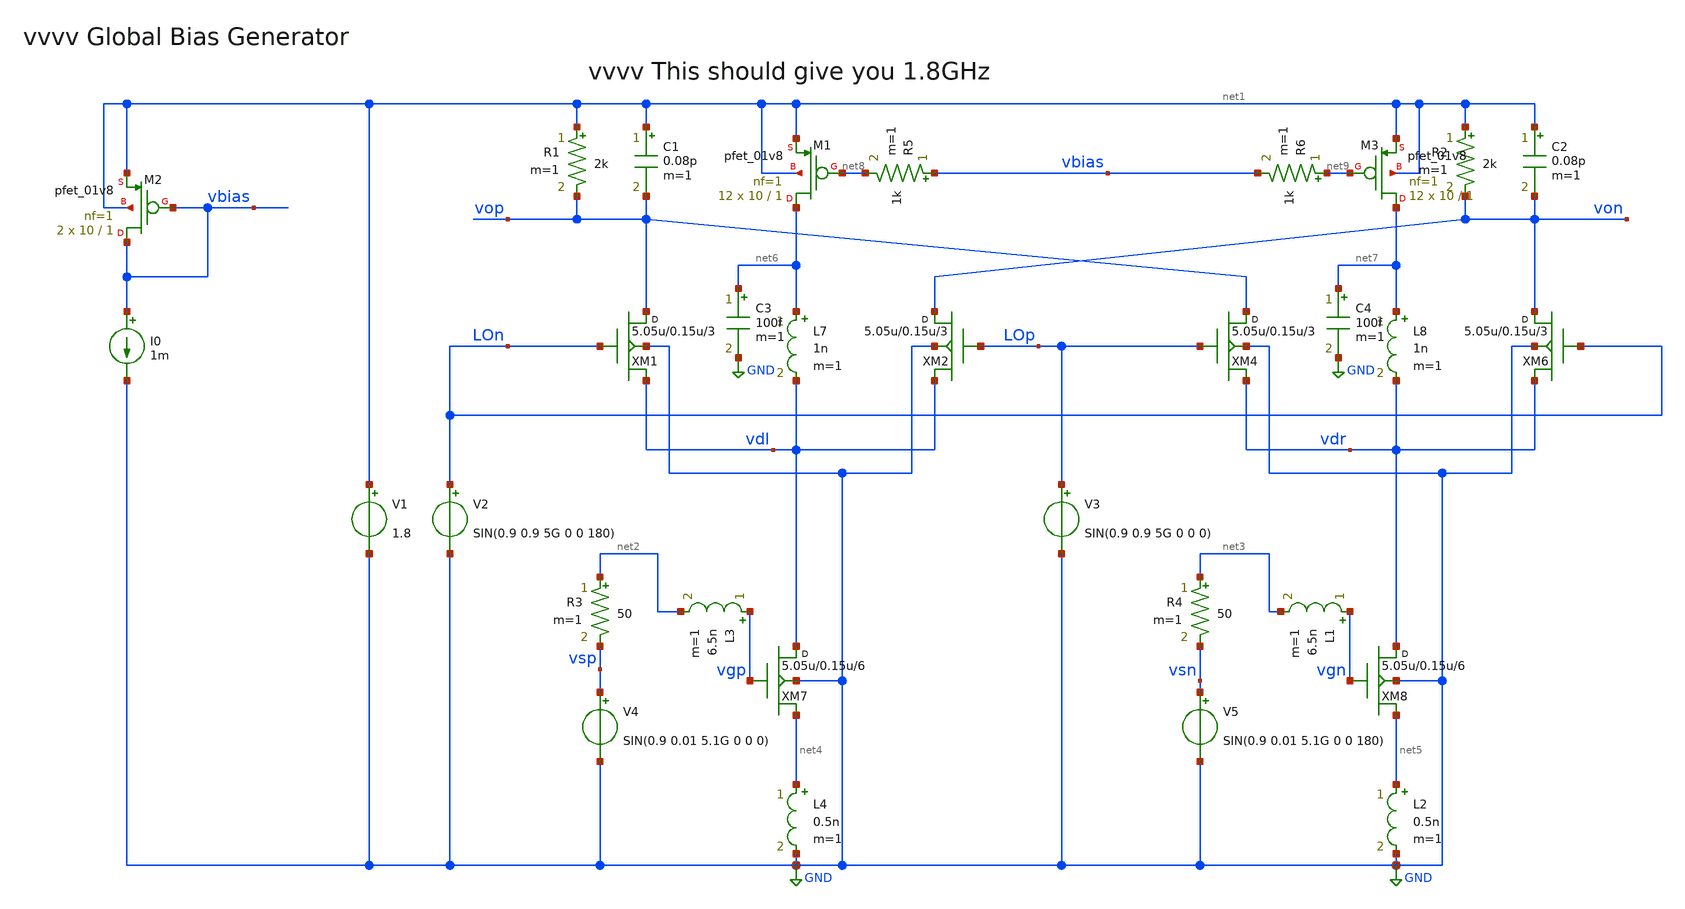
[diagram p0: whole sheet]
** sch_path: xschem/MIXER_5G_sweep.sch
**.subckt MIXER_5G_sweep
XM1 vop LOn vdl GND sky130_fd_pr__rf_nfet_01v8_bM04W5p00L0p15_ext w=5.05u l=0.15u m=3
XM2 von LOp vdl GND sky130_fd_pr__rf_nfet_01v8_bM04W5p00L0p15_ext w=5.05u l=0.15u m=3
C1 net1 vop 0.08p m=1
R1 net1 vop 2k m=1
C2 net1 von 0.08p m=1
R2 net1 von 2k m=1
V1 net1 GND 1.8
V2 LOn GND SIN(0.9 0.9 5G 0 0 180)
V3 LOp GND SIN(0.9 0.9 5G 0 0 0)
V4 vsp GND SIN(0.9 0.01 5.1G 0 0 0)
XM4 vop LOp vdr GND sky130_fd_pr__rf_nfet_01v8_bM04W5p00L0p15_ext w=5.05u l=0.15u m=3
XM6 von LOn vdr GND sky130_fd_pr__rf_nfet_01v8_bM04W5p00L0p15_ext w=5.05u l=0.15u m=3
V5 vsn GND SIN(0.9 0.01 5.1G 0 0 180)
L3 vgp net2 6.5n m=1
L1 vgn net3 6.5n m=1
L2 net5 GND 0.5n m=1
L4 net4 GND 0.5n m=1
R3 net2 vsp 50 m=1
R4 net3 vsn 50 m=1
XM7 vdl vgp net4 GND sky130_fd_pr__rf_nfet_01v8_bM04W5p00L0p15_ext w=5.05u l=0.15u m=6
XM8 vdr vgn net5 GND sky130_fd_pr__rf_nfet_01v8_bM04W5p00L0p15_ext w=5.05u l=0.15u m=6
L7 net6 vdl 1n m=1
C3 net6 GND 100f m=1
L8 net7 vdr 1n m=1
C4 net7 GND 100f m=1
XM2 vbias vbias net1 net1 sky130_fd_pr__pfet_01v8 L=1 W=10 nf=1 ad='int((nf+1)/2) * W/nf * 0.29' as='int((nf+2)/2) * W/nf * 0.29'
+ pd='2*int((nf+1)/2) * (W/nf + 0.29)' ps='2*int((nf+2)/2) * (W/nf + 0.29)' nrd='0.29 / W' nrs='0.29 / W'
+ sa=0 sb=0 sd=0 mult=2 m=2
I0 vbias GND 1m
XM1 net6 net8 net1 net1 sky130_fd_pr__pfet_01v8 L=1 W=10 nf=1 ad='int((nf+1)/2) * W/nf * 0.29' as='int((nf+2)/2) * W/nf * 0.29'
+ pd='2*int((nf+1)/2) * (W/nf + 0.29)' ps='2*int((nf+2)/2) * (W/nf + 0.29)' nrd='0.29 / W' nrs='0.29 / W'
+ sa=0 sb=0 sd=0 mult=12 m=12
R5 vbias net8 1k m=1
XM3 net7 net9 net1 net1 sky130_fd_pr__pfet_01v8 L=1 W=10 nf=1 ad='int((nf+1)/2) * W/nf * 0.29' as='int((nf+2)/2) * W/nf * 0.29'
+ pd='2*int((nf+1)/2) * (W/nf + 0.29)' ps='2*int((nf+2)/2) * (W/nf + 0.29)' nrd='0.29 / W' nrs='0.29 / W'
+ sa=0 sb=0 sd=0 mult=12 m=12
R6 net9 vbias 1k m=1
**** begin user architecture code


.subckt sky130_fd_pr__rf_nfet_01v8_bM04W5p00L0p15_ext DRAIN GATE SOURCE SUBSTRATE
X0 DRAIN GATE SOURCE SUBSTRATE sky130_fd_pr__nfet_01v8 ad=2.828e+12p pd=2.132e+07u as=4.242e+12p
+ ps=3.198e+07u w=5.05e+06u l=150000u
X1 SOURCE SUBSTRATE SUBSTRATE SUBSTRATE sky130_fd_pr__nfet_01v8 ad=0p pd=0u as=3.03e+12p
+ ps=2.14e+07u w=5.05e+06u l=150000u
X2 SOURCE GATE DRAIN SUBSTRATE sky130_fd_pr__nfet_01v8 ad=0p pd=0u as=0p ps=0u w=5.05e+06u l=150000u
X3 DRAIN GATE SOURCE SUBSTRATE sky130_fd_pr__nfet_01v8 ad=0p pd=0u as=0p ps=0u w=5.05e+06u l=150000u
X4 SUBSTRATE SUBSTRATE SOURCE SUBSTRATE sky130_fd_pr__nfet_01v8 ad=0p pd=0u as=0p ps=0u w=5.05e+06u
+ l=150000u
X5 SOURCE GATE DRAIN SUBSTRATE sky130_fd_pr__nfet_01v8 ad=0p pd=0u as=0p ps=0u w=5.05e+06u l=150000u
.ends
* .options savecurrents
.tran 10ps 50ns
.control
* run
* display
let m_start = 9
let m_stop  = 14
let m_delta = 1
let vo = v(vop)-v(von)
let vs = v(vsp)-v(vsn)
let vg = v(vgp)-v(vgn)

let m_var = m_start
while m_var le m_stop
  print m_var
  alter @m.xm1.msky130_fd_pr__pfet_01v8[m] = m_var
  alter @m.xm3.msky130_fd_pr__pfet_01v8[m] = m_var

  tran 10ps 50ns
  * plot v(von) v(vop)
  let vo = v(vop)-v(von)
  plot @l7[i]
  plot vo
  let m_var = m_var + m_delta
end


* plot vo
* plot vs
* plot vg
* fft vo vs vg
* plot db(vo) db(vs)



.endc


.lib $::SKYWATER_MODELS/sky130.lib.spice tt
* .include $::PDKPATH/libs.ref/sky130_fd_sc_hvl/spice/sky130_fd_sc_hvl.spice

**** end user architecture code
**.ends
.GLOBAL GND
.end
